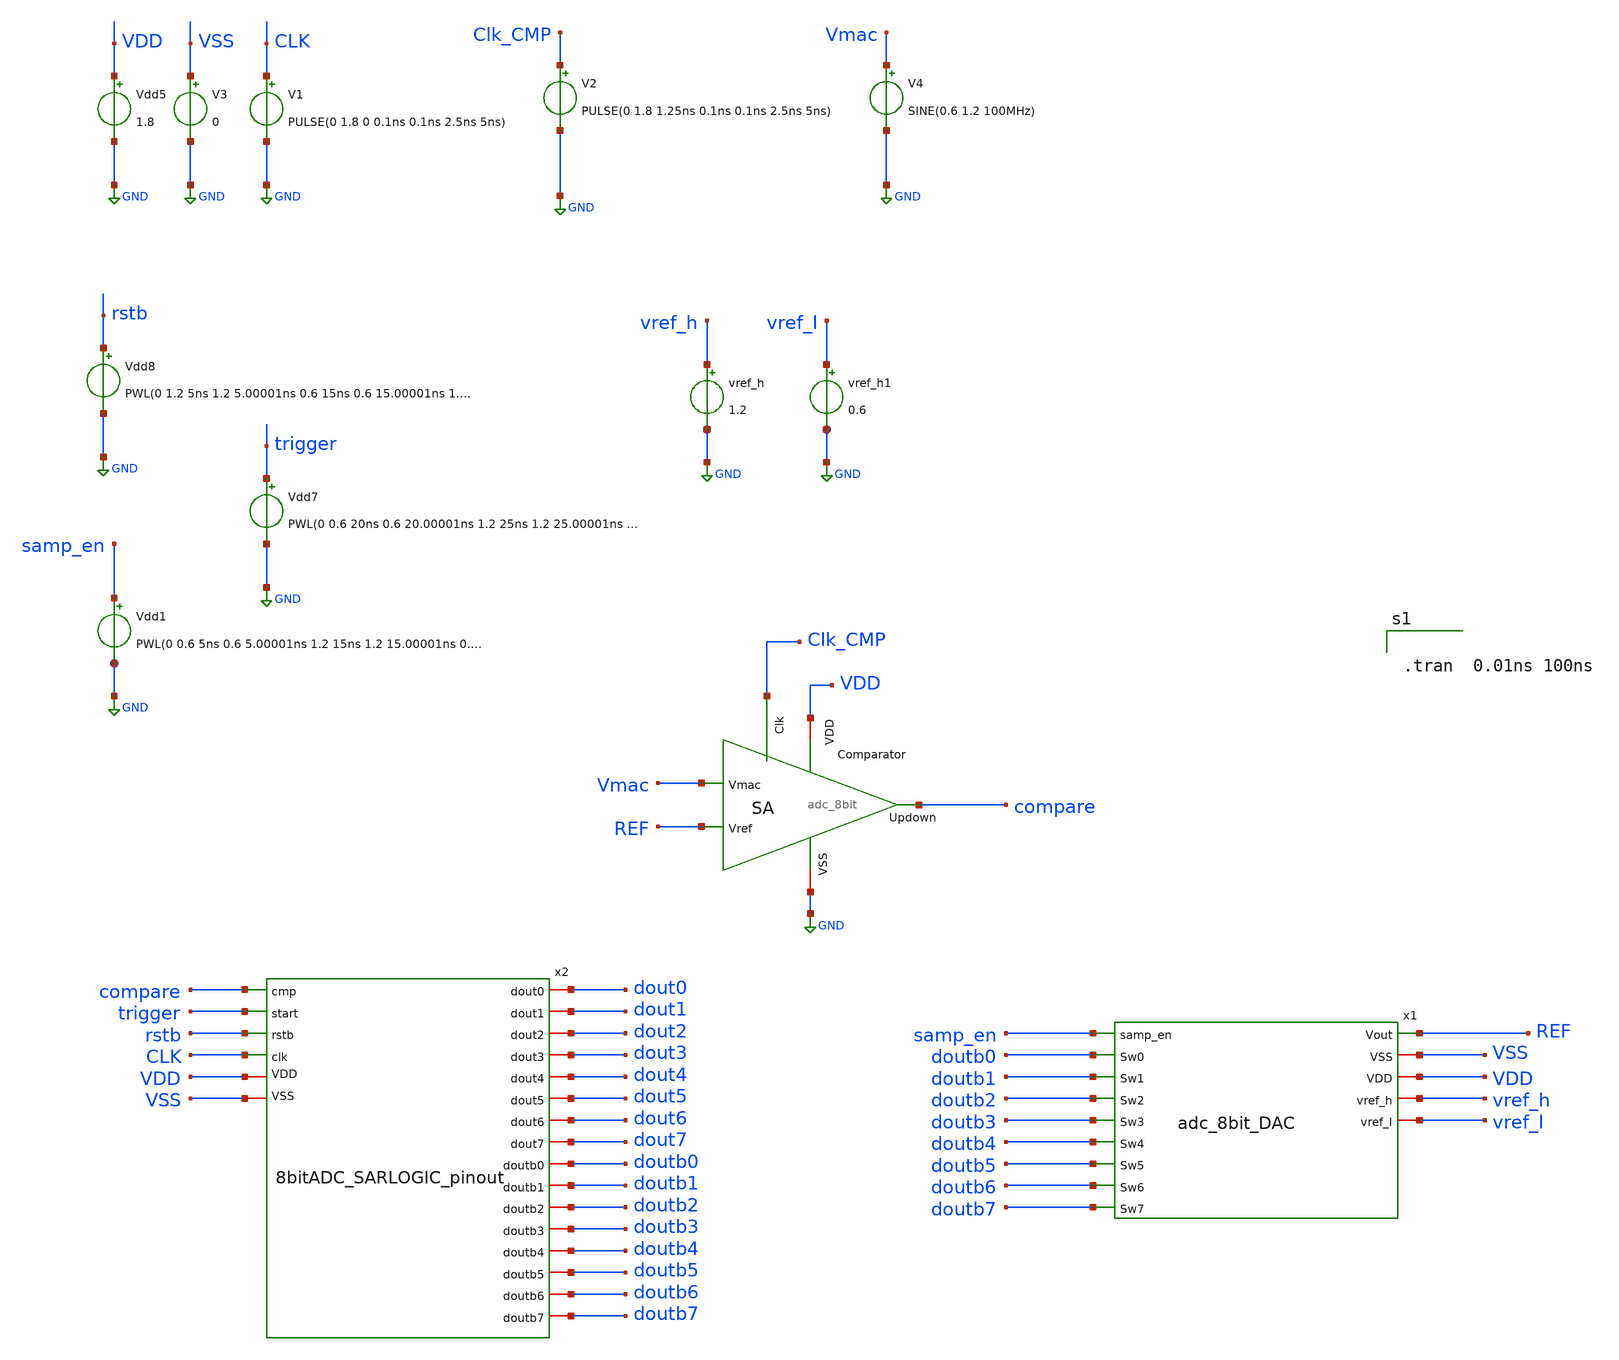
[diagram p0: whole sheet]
** sch_path: ADC_TB.sch
**.subckt ADC_TB
x1 REF VSS samp_en doutb0 VDD doutb1 vref_h doutb2 vref_l doutb3 doutb4 doutb5 doutb6 doutb7
+ adc_8bit_DAC
vref_h vref_h GND 1.2
Vdd5 VDD GND 1.8
V1 CLK GND PULSE(0 1.8 0 0.1ns 0.1ns 2.5ns 5ns)
V3 VSS GND 0
Vdd7 trigger GND PWL(0 0.6 20ns 0.6 20.00001ns 1.2 25ns 1.2 25.00001ns 0.6 )
Vdd8 rstb GND PWL(0 1.2 5ns 1.2 5.00001ns 0.6 15ns 0.6 15.00001ns 1.2 )
x3 GND VDD REF Clk_CMP Vmac compare adc_8bit
V4 Vmac GND SINE(0.6 1.2 100MHz)
V2 Clk_CMP GND PULSE(0 1.8 1.25ns 0.1ns 0.1ns 2.5ns 5ns)
Vdd1 samp_en GND PWL(0 0.6 5ns 0.6 5.00001ns 1.2 15ns 1.2 15.00001ns 0.6 )
vref_h1 vref_l GND 0.6
x2 VDD compare VSS trigger doutb0 dout0 rstb CLK doutb1 dout1 doutb2 dout2 dout3 doutb3 dout4 doutb4
+ dout5 doutb5 dout6 doutb6 doutb7 dout7 8bitADC_SARLOGIC_pinout
**** begin user architecture code

** opencircuitdesign pdks install
.lib $::SKYWATER_MODELS/sky130.lib.spice tt
.include $::SKYWATER_STDCELLS/sky130_fd_sc_hd.spice



.tran  0.01ns 100ns



**** end user architecture code
**.ends
.GLOBAL GND
.end
